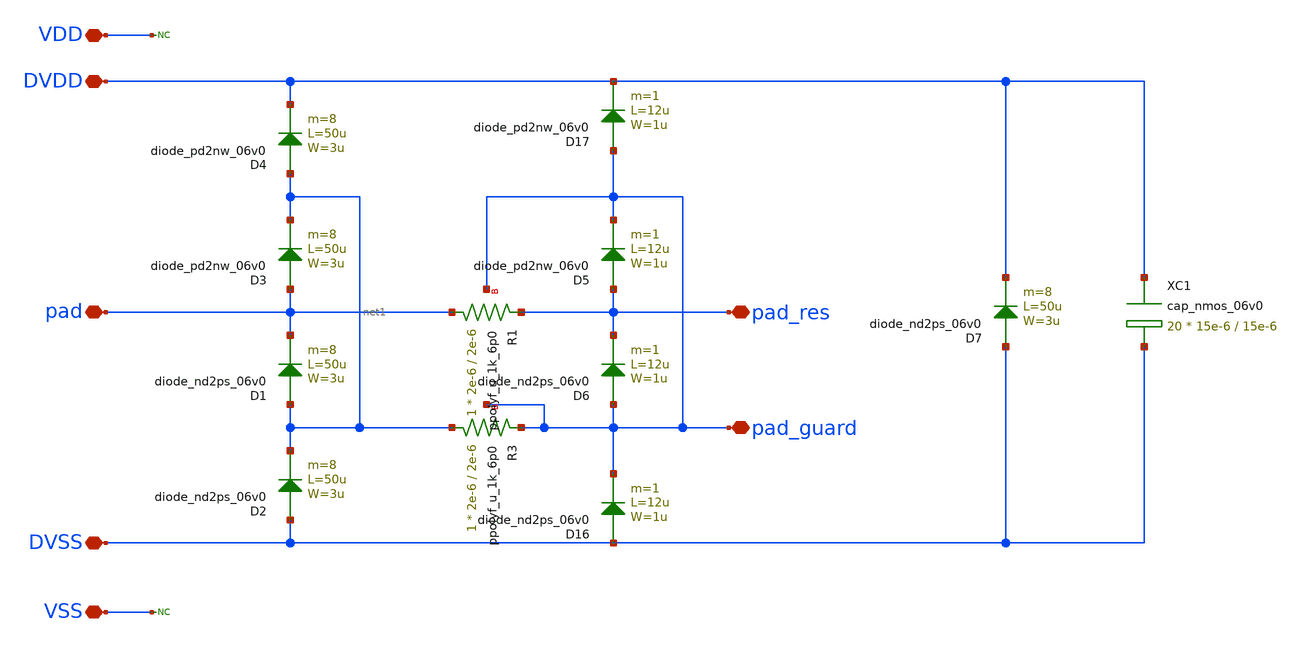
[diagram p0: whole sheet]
** sch_path: gf180mcuD/xschem/gf180mcu_liplib__asig_guard_5p0_pad_70x100.sch
**.subckt gf180mcu_liplib__asig_guard_5p0_pad_70x100 pad pad_guard DVDD DVSS pad_res VDD VSS
*.iopin pad
*.iopin pad_guard
*.iopin DVDD
*.iopin DVSS
*.iopin pad_res
*.iopin VDD
*.iopin VSS
D1 net1 pad diode_nd2ps_06v0 area='3u * 50u ' pj='2*3u + 2*50u ' m=8
D2 DVSS net1 diode_nd2ps_06v0 area='3u * 50u ' pj='2*3u + 2*50u ' m=8
D3 pad net1 diode_pd2nw_06v0 area='3u * 50u ' pj='2*3u + 2*50u ' m=8
D4 net1 DVDD diode_pd2nw_06v0 area='3u * 50u ' pj='2*3u + 2*50u ' m=8
D7 DVSS DVDD diode_nd2ps_06v0 area='3u * 50u ' pj='2*3u + 2*50u ' m=8
XC1 DVDD DVSS cap_nmos_06v0 c_width=15e-6 c_length=15e-6 m=20
D16 DVSS pad_guard diode_nd2ps_06v0 area='1u * 12u ' pj='2*1u + 2*12u ' m=1
D17 pad_guard DVDD diode_pd2nw_06v0 area='1u * 12u ' pj='2*1u + 2*12u ' m=1
D6 pad_guard pad_res diode_nd2ps_06v0 area='1u * 12u ' pj='2*1u + 2*12u ' m=1
D5 pad_res pad_guard diode_pd2nw_06v0 area='1u * 12u ' pj='2*1u + 2*12u ' m=1
XR3 net1 pad_guard pad_guard ppolyf_u_1k_6p0 r_width=2e-6 r_length=2e-6 m=1
XR1 pad pad_res pad_guard ppolyf_u_1k_6p0 r_width=2e-6 r_length=2e-6 m=1
* noconn VDD
* noconn VSS
**.ends
.end
